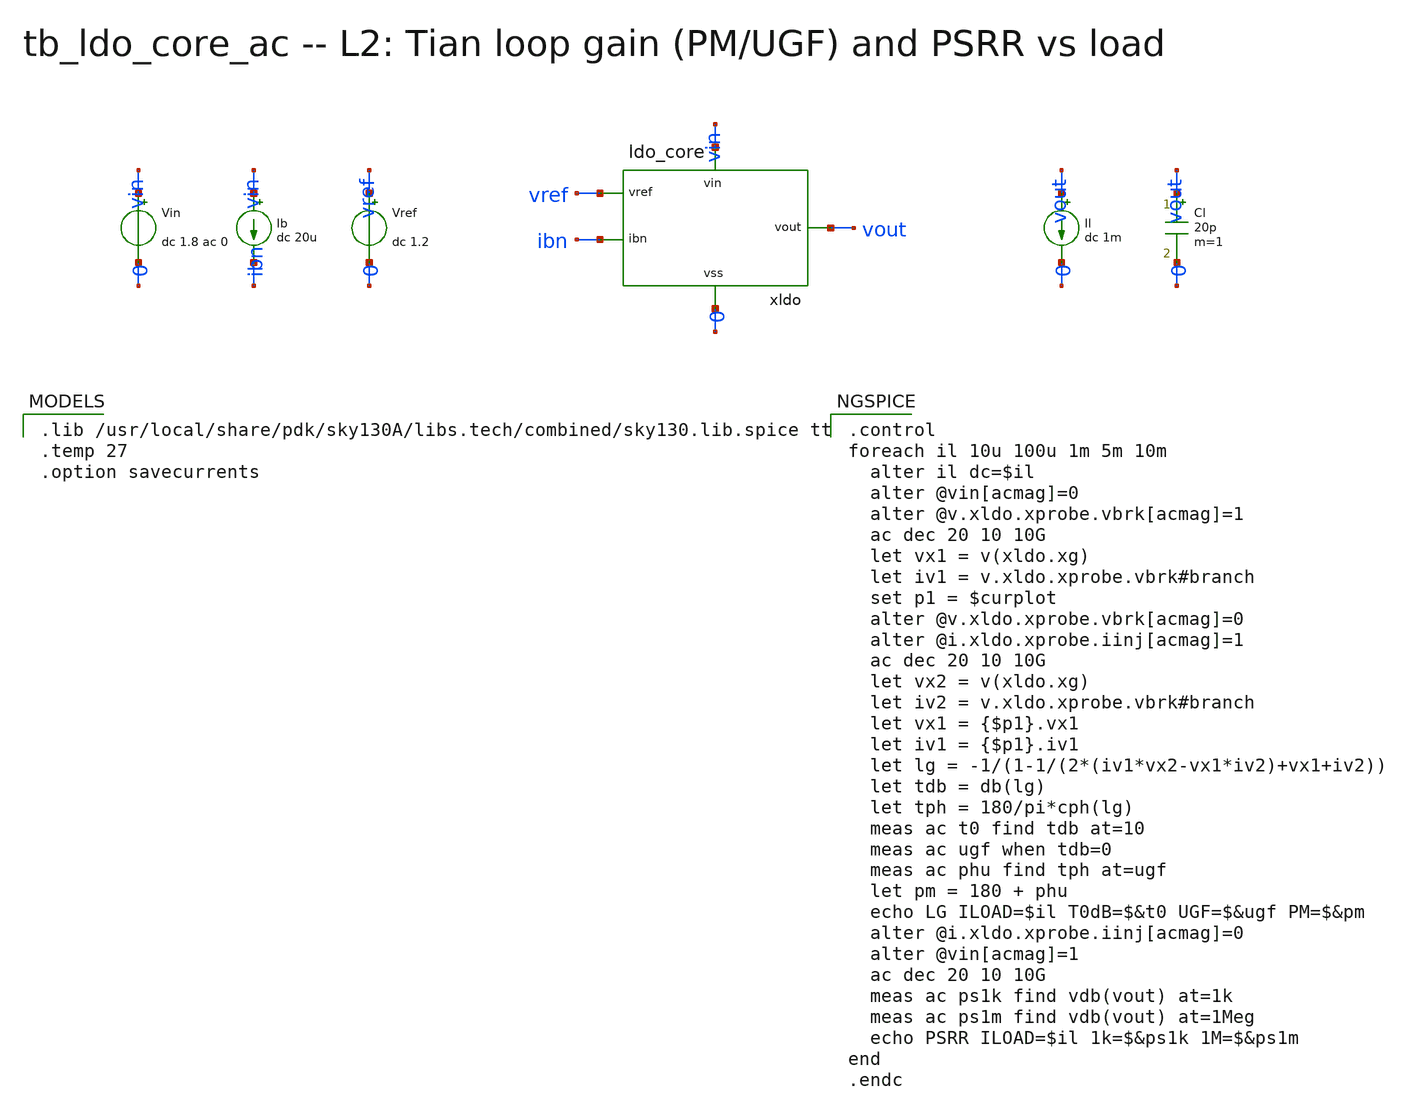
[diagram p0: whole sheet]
** sch_path: xschem/onetops_tb/tb_ldo_core_ac.sch
**.subckt tb_ldo_core_ac
Vin vin 0 dc 1.8 ac 0
Ib vin ibn dc 20u
Vref vref 0 dc 1.2
xldo vref ibn vout vin 0 ldo_core
Il vout 0 dc 1m
Cl vout 0 20p m=1
**** begin user architecture code

.lib /usr/local/share/pdk/sky130A/libs.tech/combined/sky130.lib.spice tt
.temp 27
.option savecurrents


.control
foreach il 10u 100u 1m 5m 10m
  alter il dc=$il
  alter @vin[acmag]=0
  alter @v.xldo.xprobe.vbrk[acmag]=1
  ac dec 20 10 10G
  let vx1 = v(xldo.xg)
  let iv1 = v.xldo.xprobe.vbrk#branch
  set p1 = $curplot
  alter @v.xldo.xprobe.vbrk[acmag]=0
  alter @i.xldo.xprobe.iinj[acmag]=1
  ac dec 20 10 10G
  let vx2 = v(xldo.xg)
  let iv2 = v.xldo.xprobe.vbrk#branch
  let vx1 = {$p1}.vx1
  let iv1 = {$p1}.iv1
  let lg = -1/(1-1/(2*(iv1*vx2-vx1*iv2)+vx1+iv2))
  let tdb = db(lg)
  let tph = 180/pi*cph(lg)
  meas ac t0 find tdb at=10
  meas ac ugf when tdb=0
  meas ac phu find tph at=ugf
  let pm = 180 + phu
  echo LG ILOAD=$il T0dB=$&t0 UGF=$&ugf PM=$&pm
  alter @i.xldo.xprobe.iinj[acmag]=0
  alter @vin[acmag]=1
  ac dec 20 10 10G
  meas ac ps1k find vdb(vout) at=1k
  meas ac ps1m find vdb(vout) at=1Meg
  echo PSRR ILOAD=$il 1k=$&ps1k 1M=$&ps1m
end
.endc

**** end user architecture code
**.ends

* expanding   symbol:  onetops/ldo_core.sym # of pins=5
** sym_path: xschem/onetops/ldo_core.sym
** sch_path: xschem/onetops/ldo_core.sch
.subckt ldo_core vref ibn vout vin vss
*.ipin vref
*.ipin ibn
*.iopin vout
*.iopin vin
*.iopin vss
xbias ibn x vout i_pd i_tail vss bias_mirror
xvset vref i_pd i_tail vset vin vset_gen
xfvf vset x vout fvf_core
xprobe x xg lg_probe
xpass xg vout vin pass_pmos
xcomp x vout comp_rc
.ends


* expanding   symbol:  onetops/bias_mirror.sym # of pins=6
** sym_path: xschem/onetops/bias_mirror.sym
** sch_path: xschem/onetops/bias_mirror.sch
.subckt bias_mirror ibn o_fvf o_bl o_pd o_tail vss
*.ipin ibn
*.opin o_fvf
*.opin o_bl
*.opin o_pd
*.opin o_tail
*.iopin vss
XMN0 ibn ibn vss vss sky130_fd_pr__nfet_01v8 L=1 W=4 nf=1 ad='int((1 + 1)/2) * 4 / 1 * 0.29' as='int((1 + 2)/2) * 4 / 1 * 0.29'
+ pd='2*int((1 + 1)/2) * (4 / 1 + 0.29)' ps='2*int((1 + 2)/2) * (4 / 1 + 0.29)' nrd='0.29 / 4 ' nrs='0.29 / 4 '
+ sa=0 sb=0 sd=0 mult=1 m=1
XMN1 o_fvf ibn vss vss sky130_fd_pr__nfet_01v8 L=1 W=4 nf=1 ad='int((1 + 1)/2) * 4 / 1 * 0.29' as='int((1 + 2)/2) * 4 / 1 * 0.29'
+ pd='2*int((1 + 1)/2) * (4 / 1 + 0.29)' ps='2*int((1 + 2)/2) * (4 / 1 + 0.29)' nrd='0.29 / 4 ' nrs='0.29 / 4 '
+ sa=0 sb=0 sd=0 mult=1 m=1
XMN2 o_bl ibn vss vss sky130_fd_pr__nfet_01v8 L=1 W=4 nf=1 ad='int((1 + 1)/2) * 4 / 1 * 0.29' as='int((1 + 2)/2) * 4 / 1 * 0.29'
+ pd='2*int((1 + 1)/2) * (4 / 1 + 0.29)' ps='2*int((1 + 2)/2) * (4 / 1 + 0.29)' nrd='0.29 / 4 ' nrs='0.29 / 4 '
+ sa=0 sb=0 sd=0 mult=5 m=5
XMN3 o_pd ibn vss vss sky130_fd_pr__nfet_01v8 L=1 W=4 nf=1 ad='int((1 + 1)/2) * 4 / 1 * 0.29' as='int((1 + 2)/2) * 4 / 1 * 0.29'
+ pd='2*int((1 + 1)/2) * (4 / 1 + 0.29)' ps='2*int((1 + 2)/2) * (4 / 1 + 0.29)' nrd='0.29 / 4 ' nrs='0.29 / 4 '
+ sa=0 sb=0 sd=0 mult=1 m=1
XMN4 o_tail ibn vss vss sky130_fd_pr__nfet_01v8 L=1 W=4 nf=1 ad='int((1 + 1)/2) * 4 / 1 * 0.29' as='int((1 + 2)/2) * 4 / 1 * 0.29'
+ pd='2*int((1 + 1)/2) * (4 / 1 + 0.29)' ps='2*int((1 + 2)/2) * (4 / 1 + 0.29)' nrd='0.29 / 4 ' nrs='0.29 / 4 '
+ sa=0 sb=0 sd=0 mult=2 m=2
.ends


* expanding   symbol:  onetops/vset_gen.sym # of pins=5
** sym_path: xschem/onetops/vset_gen.sym
** sch_path: xschem/onetops/vset_gen.sch
.subckt vset_gen vref i_pd i_tail vset vin
*.ipin vref
*.opin vset
*.iopin i_pd
*.iopin i_tail
*.iopin vin
XMPD i_pd i_pd vin vin sky130_fd_pr__pfet_01v8_lvt L=2 W=10 nf=1 ad='int((1 + 1)/2) * 10 / 1 * 0.29'
+ as='int((1 + 2)/2) * 10 / 1 * 0.29' pd='2*int((1 + 1)/2) * (10 / 1 + 0.29)' ps='2*int((1 + 2)/2) * (10 / 1 + 0.29)'
+ nrd='0.29 / 10 ' nrs='0.29 / 10 ' sa=0 sb=0 sd=0 mult=1 m=1
XMPS vrep i_pd vin vin sky130_fd_pr__pfet_01v8_lvt L=2 W=10 nf=1 ad='int((1 + 1)/2) * 10 / 1 * 0.29'
+ as='int((1 + 2)/2) * 10 / 1 * 0.29' pd='2*int((1 + 1)/2) * (10 / 1 + 0.29)' ps='2*int((1 + 2)/2) * (10 / 1 + 0.29)'
+ nrd='0.29 / 10 ' nrs='0.29 / 10 ' sa=0 sb=0 sd=0 mult=1 m=1
XMR 0 vset vrep vrep sky130_fd_pr__pfet_01v8_lvt L=1 W=100 nf=1 ad='int((1 + 1)/2) * 100 / 1 * 0.29'
+ as='int((1 + 2)/2) * 100 / 1 * 0.29' pd='2*int((1 + 1)/2) * (100 / 1 + 0.29)' ps='2*int((1 + 2)/2) * (100 / 1 + 0.29)'
+ nrd='0.29 / 100 ' nrs='0.29 / 100 ' sa=0 sb=0 sd=0 mult=1 m=1
xota vref vrep i_tail vset vin ota5t
Cset vset 0 2p m=1
.ends


* expanding   symbol:  onetops/fvf_core.sym # of pins=3
** sym_path: xschem/onetops/fvf_core.sym
** sch_path: xschem/onetops/fvf_core.sch
.subckt fvf_core vset x vout
*.ipin vset
*.opin x
*.iopin vout
XMC x vset vout vout sky130_fd_pr__pfet_01v8_lvt L=1 W=100 nf=1 ad='int((1 + 1)/2) * 100 / 1 * 0.29'
+ as='int((1 + 2)/2) * 100 / 1 * 0.29' pd='2*int((1 + 1)/2) * (100 / 1 + 0.29)' ps='2*int((1 + 2)/2) * (100 / 1 + 0.29)'
+ nrd='0.29 / 100 ' nrs='0.29 / 100 ' sa=0 sb=0 sd=0 mult=1 m=1
.ends


* expanding   symbol:  onetops/lg_probe.sym # of pins=2
** sym_path: xschem/onetops/lg_probe.sym
** sch_path: xschem/onetops/lg_probe.sch
.subckt lg_probe drv lin
*.iopin drv
*.iopin lin
Vbrk lin drv dc 0 ac 0
Iinj 0 lin dc 0 ac 0
.ends


* expanding   symbol:  onetops/pass_pmos.sym # of pins=3
** sym_path: xschem/onetops/pass_pmos.sym
** sch_path: xschem/onetops/pass_pmos.sch
.subckt pass_pmos g vout vin
*.ipin g
*.iopin vin
*.iopin vout
XMP vout g vin vin sky130_fd_pr__pfet_01v8 L=0.35 W=10 nf=1 ad='int((1 + 1)/2) * 10 / 1 * 0.29' as='int((1 + 2)/2) * 10 / 1 * 0.29'
+ pd='2*int((1 + 1)/2) * (10 / 1 + 0.29)' ps='2*int((1 + 2)/2) * (10 / 1 + 0.29)' nrd='0.29 / 10 ' nrs='0.29 / 10 '
+ sa=0 sb=0 sd=0 mult=70 m=70
.ends


* expanding   symbol:  onetops/comp_rc.sym # of pins=2
** sym_path: xschem/onetops/comp_rc.sym
** sch_path: xschem/onetops/comp_rc.sch
.subckt comp_rc a b
*.iopin a
*.iopin b
Rz a n1 1 m=1
Cc n1 b 4p m=1
.ends


* expanding   symbol:  onetops/ota5t.sym # of pins=5
** sym_path: xschem/onetops/ota5t.sym
** sch_path: xschem/onetops/ota5t.sch
.subckt ota5t inp inn tail out vdd
*.ipin inp
*.ipin inn
*.opin out
*.iopin tail
*.iopin vdd
XMP1 nd nd vdd vdd sky130_fd_pr__pfet_01v8_lvt L=2 W=20 nf=1 ad='int((1 + 1)/2) * 20 / 1 * 0.29' as='int((1 + 2)/2) * 20 / 1 * 0.29'
+ pd='2*int((1 + 1)/2) * (20 / 1 + 0.29)' ps='2*int((1 + 2)/2) * (20 / 1 + 0.29)' nrd='0.29 / 20 ' nrs='0.29 / 20 '
+ sa=0 sb=0 sd=0 mult=1 m=1
XMP2 out nd vdd vdd sky130_fd_pr__pfet_01v8_lvt L=2 W=20 nf=1 ad='int((1 + 1)/2) * 20 / 1 * 0.29' as='int((1 + 2)/2) * 20 / 1 * 0.29'
+ pd='2*int((1 + 1)/2) * (20 / 1 + 0.29)' ps='2*int((1 + 2)/2) * (20 / 1 + 0.29)' nrd='0.29 / 20 ' nrs='0.29 / 20 '
+ sa=0 sb=0 sd=0 mult=1 m=1
XMN1 nd inp tail 0 sky130_fd_pr__nfet_01v8 L=1 W=5 nf=1 ad='int((1 + 1)/2) * 5 / 1 * 0.29' as='int((1 + 2)/2) * 5 / 1 * 0.29'
+ pd='2*int((1 + 1)/2) * (5 / 1 + 0.29)' ps='2*int((1 + 2)/2) * (5 / 1 + 0.29)' nrd='0.29 / 5 ' nrs='0.29 / 5 '
+ sa=0 sb=0 sd=0 mult=1 m=1
XMN2 out inn tail 0 sky130_fd_pr__nfet_01v8 L=1 W=5 nf=1 ad='int((1 + 1)/2) * 5 / 1 * 0.29' as='int((1 + 2)/2) * 5 / 1 * 0.29'
+ pd='2*int((1 + 1)/2) * (5 / 1 + 0.29)' ps='2*int((1 + 2)/2) * (5 / 1 + 0.29)' nrd='0.29 / 5 ' nrs='0.29 / 5 '
+ sa=0 sb=0 sd=0 mult=1 m=1
.ends

.end
